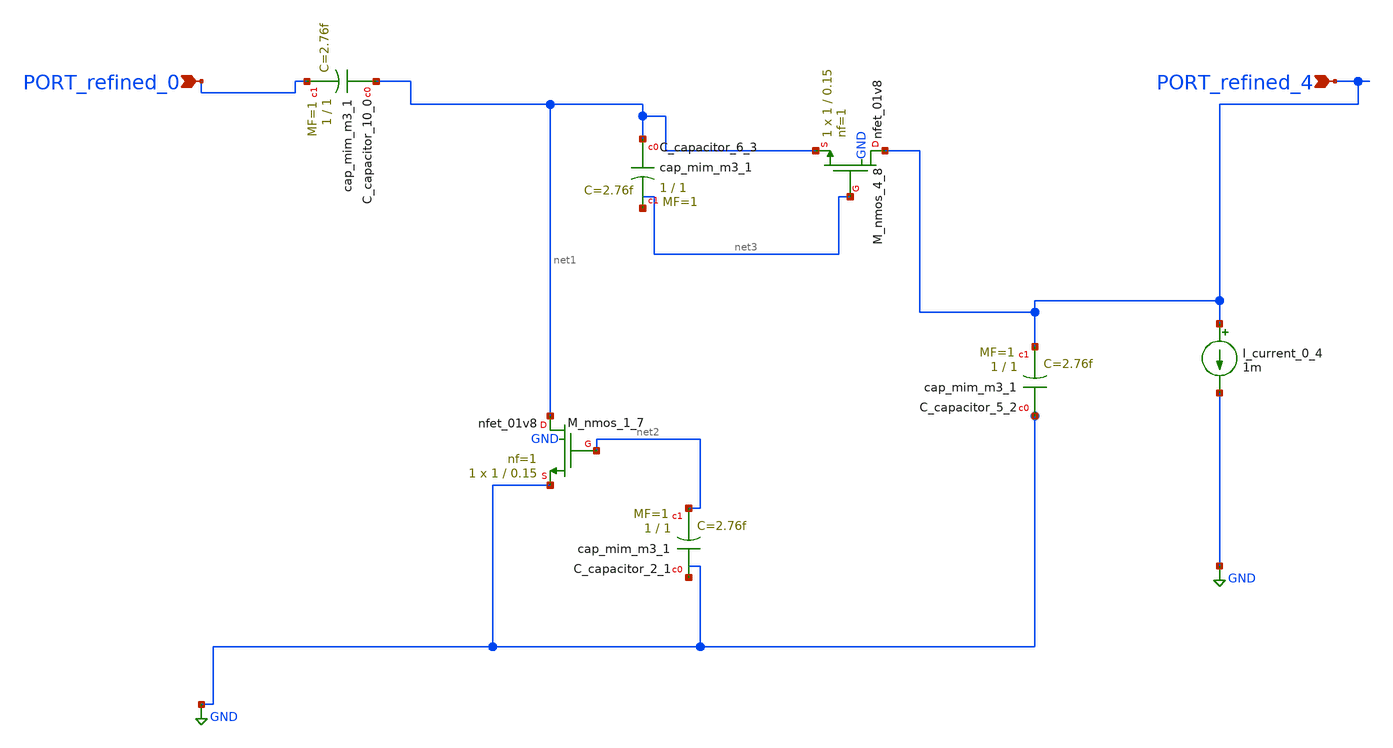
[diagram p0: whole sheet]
** sch_path: schematics/10_1109_ACCESS_2021_3098895_06_003.sch
**.subckt 10_1109_ACCESS_2021_3098895_06_003 PORT_refined_4 PORT_refined_0
*.ipin PORT_refined_4
*.ipin PORT_refined_0
XC_capacitor_10_0 net1 PORT_refined_0 sky130_fd_pr__cap_mim_m3_1 W=1 L=1 MF=1 m=1
XC_capacitor_2_1 GND net2 sky130_fd_pr__cap_mim_m3_1 W=1 L=1 MF=1 m=1
XC_capacitor_5_2 GND PORT_refined_4 sky130_fd_pr__cap_mim_m3_1 W=1 L=1 MF=1 m=1
XC_capacitor_6_3 net1 net3 sky130_fd_pr__cap_mim_m3_1 W=1 L=1 MF=1 m=1
I_current_0_4 PORT_refined_4 GND 1m
XM_nmos_1_7 net1 net2 GND GND sky130_fd_pr__nfet_01v8 L=0.15 W=1 nf=1 ad='int((1 + 1)/2) * 1 / 1 * 0.29'
+ as='int((1 + 2)/2) * 1 / 1 * 0.29' pd='2*int((1 + 1)/2) * (1 / 1 + 0.29)' ps='2*int((1 + 2)/2) * (1 / 1 + 0.29)'
+ nrd='0.29 / 1 ' nrs='0.29 / 1 ' sa=0 sb=0 sd=0 mult=1 m=1
XM_nmos_4_8 PORT_refined_4 net3 net1 GND sky130_fd_pr__nfet_01v8 L=0.15 W=1 nf=1 ad='int((1 + 1)/2) * 1 / 1 * 0.29'
+ as='int((1 + 2)/2) * 1 / 1 * 0.29' pd='2*int((1 + 1)/2) * (1 / 1 + 0.29)' ps='2*int((1 + 2)/2) * (1 / 1 + 0.29)'
+ nrd='0.29 / 1 ' nrs='0.29 / 1 ' sa=0 sb=0 sd=0 mult=1 m=1
**.ends
.GLOBAL GND
.end
